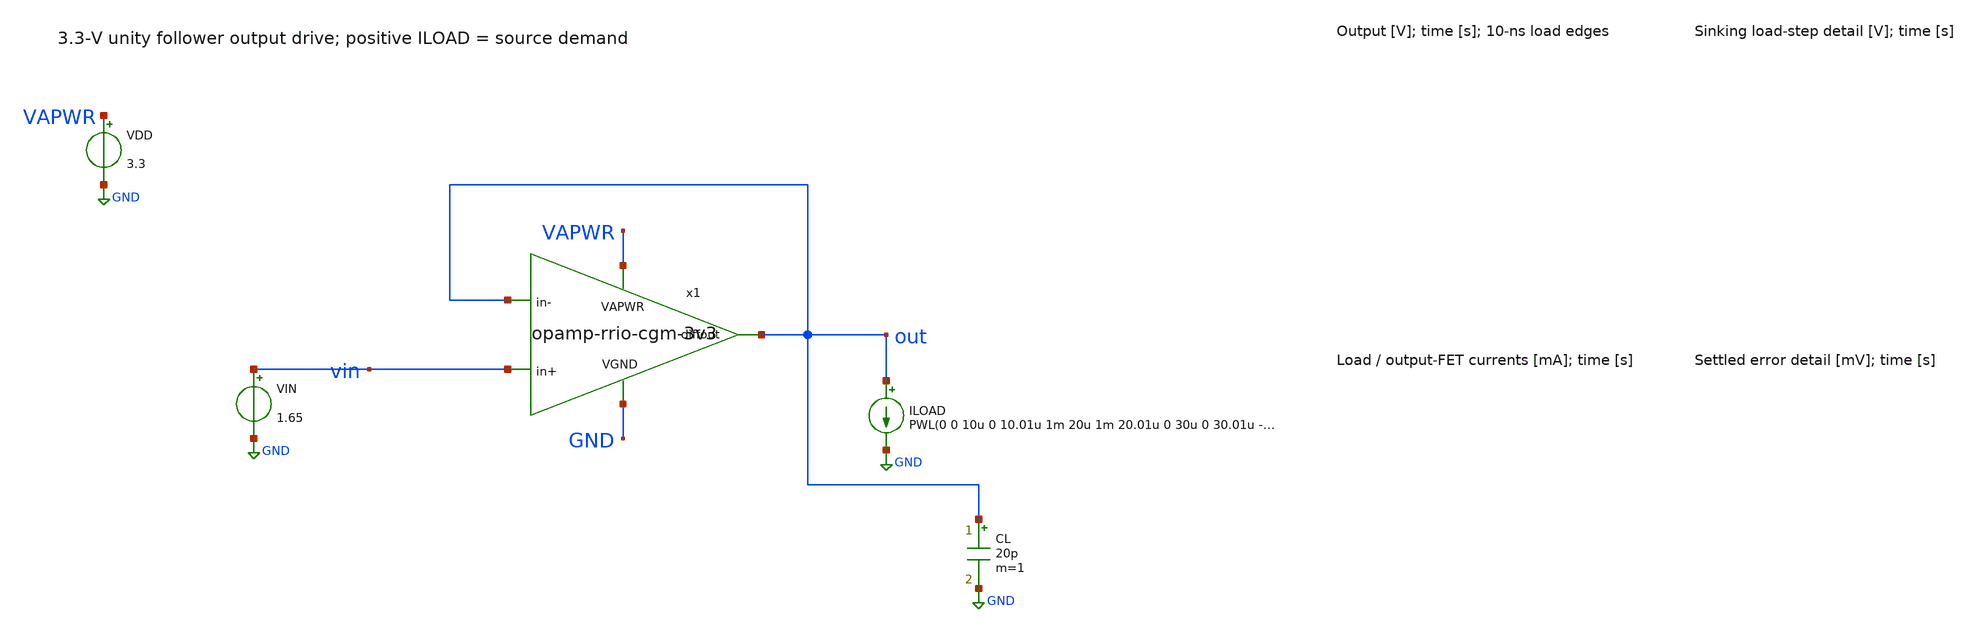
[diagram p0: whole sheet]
** sch_path: xschem/testbench_output_tran_3v3.sch
**.subckt testbench_output_tran_3v3
x1 VAPWR out vin out GND opamp-rrio-cgm-3v3
VDD VAPWR GND 3.3
VIN vin GND 1.65
ILOAD out GND PWL(0 0 10u 0 10.01u 1m 20u 1m 20.01u 0 30u 0 30.01u -1m 40u -1m 40.01u 0 50u 0)
CL out GND 20p m=1
**** begin user architecture code
 .lib $::SKYWATER_MODELS/sky130.lib.spice tt

.options klu itl1=100 reltol=.0001
.nodeset v(x1.net1)=2.55229105
.nodeset v(x1.net3)=0.866789395
.nodeset v(x1.net4)=0.29731059
.nodeset v(x1.net5)=0.297227056
.nodeset v(x1.net10)=2.03109432
.nodeset v(x1.net12)=1.08535928
.nodeset v(x1.net6)=2.02894826
.nodeset v(x1.net13)=1.08255405
.nodeset v(x1.bias1)=2.05405688
.nodeset v(x1.bias2)=2.04452255
.nodeset v(x1.bias3)=1.14047666
.nodeset v(x1.bias4)=1.04710014
.nodeset v(x1.bias)=1.65
.nodeset v(out)=1.65 v(x1.xb.xref.vbiasn)=.91 v(x1.xb.xref.vbiasp)=2.05 v(x1.xb.xref.vstartup)=.1
.control
set wr_singlescale
set wr_vecnames
save all @iload[current] @m.x1.xm29.msky130_fd_pr__pfet_g5v0d10v5[id]
+ @m.x1.xm32.msky130_fd_pr__nfet_g5v0d10v5[id] @m.x1.xb.xref.xm1.msky130_fd_pr__pfet_g5v0d10v5[id]
tran 5n 50u 0 5n

* Reject roots outside the SKY130 HV gate-voltage range.
let physical_bias_peak = vecmax(abs(v(x1.bias)))
if physical_bias_peak > 5.5
echo PHYSICAL_BIAS_ERROR: invalid PDK operating point
quit 1
end
let error_mV=1000*(v(out)-v(vin))
let load_mA=1000*@iload[current]
let source_mA=1000*@m.x1.xm29.msky130_fd_pr__pfet_g5v0d10v5[id]
let sink_mA=1000*@m.x1.xm32.msky130_fd_pr__nfet_g5v0d10v5[id]
write testbench_output_tran_3v3.raw all
wrdata testbench_output_tran_3v3.dat v(vin) v(out) @iload[current] i(VDD)
+ @m.x1.xm29.msky130_fd_pr__pfet_g5v0d10v5[id] @m.x1.xm32.msky130_fd_pr__nfet_g5v0d10v5[id] @m.x1.xb.xref.xm1.msky130_fd_pr__pfet_g5v0d10v5[id]
.endc

**** end user architecture code
**.ends

* expanding   symbol:  opamp-rrio-cgm-3v3.sym # of pins=5
** sym_path: xschem/opamp-rrio-cgm-3v3.sym
** sch_path: xschem/opamp-rrio-cgm-3v3.sch
.subckt opamp-rrio-cgm-3v3 VAPWR diffout in+ in- VGND
*.ipin in-
*.ipin in+
*.opin diffout
*.iopin VAPWR
*.iopin VGND
XM1 net2 in- net3 VGND sky130_fd_pr__nfet_g5v0d10v5 L=0.5 W=69.44 nf=5 ad='int((nf+1)/2) * W/nf * 0.29'
+ as='int((nf+2)/2) * W/nf * 0.29' pd='2*int((nf+1)/2) * (W/nf + 0.29)' ps='2*int((nf+2)/2) * (W/nf + 0.29)'
+ nrd='0.29 / W' nrs='0.29 / W' sa=0 sb=0 sd=0 mult=1 m=1
XM3 drain in+ net3 VGND sky130_fd_pr__nfet_g5v0d10v5 L=0.5 W=69.44 nf=5 ad='int((nf+1)/2) * W/nf * 0.29'
+ as='int((nf+2)/2) * W/nf * 0.29' pd='2*int((nf+1)/2) * (W/nf + 0.29)' ps='2*int((nf+2)/2) * (W/nf + 0.29)'
+ nrd='0.29 / W' nrs='0.29 / W' sa=0 sb=0 sd=0 mult=1 m=1
XM7 drain bias net3 VGND sky130_fd_pr__nfet_g5v0d10v5 L=0.5 W=69.44 nf=5 ad='int((nf+1)/2) * W/nf * 0.29'
+ as='int((nf+2)/2) * W/nf * 0.29' pd='2*int((nf+1)/2) * (W/nf + 0.29)' ps='2*int((nf+2)/2) * (W/nf + 0.29)'
+ nrd='0.29 / W' nrs='0.29 / W' sa=0 sb=0 sd=0 mult=1 m=1
XM8 net2 bias net3 VGND sky130_fd_pr__nfet_g5v0d10v5 L=0.5 W=69.44 nf=5 ad='int((nf+1)/2) * W/nf * 0.29'
+ as='int((nf+2)/2) * W/nf * 0.29' pd='2*int((nf+1)/2) * (W/nf + 0.29)' ps='2*int((nf+2)/2) * (W/nf + 0.29)'
+ nrd='0.29 / W' nrs='0.29 / W' sa=0 sb=0 sd=0 mult=1 m=1
XM18 net13 bias3 net5 VGND sky130_fd_pr__nfet_g5v0d10v5 L=0.5 W=13.89 nf=1 ad='int((nf+1)/2) * W/nf * 0.29'
+ as='int((nf+2)/2) * W/nf * 0.29' pd='2*int((nf+1)/2) * (W/nf + 0.29)' ps='2*int((nf+2)/2) * (W/nf + 0.29)'
+ nrd='0.29 / W' nrs='0.29 / W' sa=0 sb=0 sd=0 mult=1 m=1
XM19 net12 bias3 net4 VGND sky130_fd_pr__nfet_g5v0d10v5 L=0.5 W=13.89 nf=1 ad='int((nf+1)/2) * W/nf * 0.29'
+ as='int((nf+2)/2) * W/nf * 0.29' pd='2*int((nf+1)/2) * (W/nf + 0.29)' ps='2*int((nf+2)/2) * (W/nf + 0.29)'
+ nrd='0.29 / W' nrs='0.29 / W' sa=0 sb=0 sd=0 mult=1 m=1
XM20 net5 net13 VGND VGND sky130_fd_pr__nfet_g5v0d10v5 L=2 W=6.66 nf=2 ad='int((nf+1)/2) * W/nf * 0.29'
+ as='int((nf+2)/2) * W/nf * 0.29' pd='2*int((nf+1)/2) * (W/nf + 0.29)' ps='2*int((nf+2)/2) * (W/nf + 0.29)'
+ nrd='0.29 / W' nrs='0.29 / W' sa=0 sb=0 sd=0 mult=1 m=1
XM21 net4 net13 VGND VGND sky130_fd_pr__nfet_g5v0d10v5 L=2 W=6.66 nf=2 ad='int((nf+1)/2) * W/nf * 0.29'
+ as='int((nf+2)/2) * W/nf * 0.29' pd='2*int((nf+1)/2) * (W/nf + 0.29)' ps='2*int((nf+2)/2) * (W/nf + 0.29)'
+ nrd='0.29 / W' nrs='0.29 / W' sa=0 sb=0 sd=0 mult=1 m=1
XM22 net3 bias4 VGND VGND sky130_fd_pr__nfet_g5v0d10v5 L=6 W=10 nf=1 ad='int((nf+1)/2) * W/nf * 0.29'
+ as='int((nf+2)/2) * W/nf * 0.29' pd='2*int((nf+1)/2) * (W/nf + 0.29)' ps='2*int((nf+2)/2) * (W/nf + 0.29)'
+ nrd='0.29 / W' nrs='0.29 / W' sa=0 sb=0 sd=0 mult=1 m=1
XM25 net8 net8 net11 VGND sky130_fd_pr__nfet_g5v0d10v5 L=0.5 W=13.89 nf=1 ad='int((nf+1)/2) * W/nf * 0.29'
+ as='int((nf+2)/2) * W/nf * 0.29' pd='2*int((nf+1)/2) * (W/nf + 0.29)' ps='2*int((nf+2)/2) * (W/nf + 0.29)'
+ nrd='0.29 / W' nrs='0.29 / W' sa=0 sb=0 sd=0 mult=1 m=1
XM26 net10 net8 net12 VGND sky130_fd_pr__nfet_g5v0d10v5 L=0.5 W=13.89 nf=1 ad='int((nf+1)/2) * W/nf * 0.29'
+ as='int((nf+2)/2) * W/nf * 0.29' pd='2*int((nf+1)/2) * (W/nf + 0.29)' ps='2*int((nf+2)/2) * (W/nf + 0.29)'
+ nrd='0.29 / W' nrs='0.29 / W' sa=0 sb=0 sd=0 mult=1 m=1
XM30 net11 net11 VGND VGND sky130_fd_pr__nfet_g5v0d10v5 L=2 W=6.66 nf=2 ad='int((nf+1)/2) * W/nf * 0.29'
+ as='int((nf+2)/2) * W/nf * 0.29' pd='2*int((nf+1)/2) * (W/nf + 0.29)' ps='2*int((nf+2)/2) * (W/nf + 0.29)'
+ nrd='0.29 / W' nrs='0.29 / W' sa=0 sb=0 sd=0 mult=1 m=1
XM31 net9 bias4 VGND VGND sky130_fd_pr__nfet_g5v0d10v5 L=6 W=10 nf=1 ad='int((nf+1)/2) * W/nf * 0.29'
+ as='int((nf+2)/2) * W/nf * 0.29' pd='2*int((nf+1)/2) * (W/nf + 0.29)' ps='2*int((nf+2)/2) * (W/nf + 0.29)'
+ nrd='0.29 / W' nrs='0.29 / W' sa=0 sb=0 sd=0 mult=1 m=1
XM32 diffout net12 VGND VGND sky130_fd_pr__nfet_g5v0d10v5 L=2 W=133.2 nf=40 ad='int((nf+1)/2) * W/nf * 0.29'
+ as='int((nf+2)/2) * W/nf * 0.29' pd='2*int((nf+1)/2) * (W/nf + 0.29)' ps='2*int((nf+2)/2) * (W/nf + 0.29)'
+ nrd='0.29 / W' nrs='0.29 / W' sa=0 sb=0 sd=0 mult=1 m=1
XC1 diffout drain sky130_fd_pr__cap_mim_m3_1 W=18 L=18 MF=1 m=1
XC2 diffout net4 sky130_fd_pr__cap_mim_m3_1 W=30 L=30 MF=1 m=1
XC2B diffout net4 sky130_fd_pr__cap_mim_m3_1 W=30 L=10 MF=1 m=1
XM13 net1 bias1 VAPWR VAPWR sky130_fd_pr__pfet_g5v0d10v5 L=6 W=33 nf=1 ad='int((nf+1)/2) * W/nf * 0.29'
+ as='int((nf+2)/2) * W/nf * 0.29' pd='2*int((nf+1)/2) * (W/nf + 0.29)' ps='2*int((nf+2)/2) * (W/nf + 0.29)'
+ nrd='0.29 / W' nrs='0.29 / W' sa=0 sb=0 sd=0 mult=1 m=1
XM14 net2 net6 VAPWR VAPWR sky130_fd_pr__pfet_g5v0d10v5 L=2 W=22 nf=2 ad='int((nf+1)/2) * W/nf * 0.29'
+ as='int((nf+2)/2) * W/nf * 0.29' pd='2*int((nf+1)/2) * (W/nf + 0.29)' ps='2*int((nf+2)/2) * (W/nf + 0.29)'
+ nrd='0.29 / W' nrs='0.29 / W' sa=0 sb=0 sd=0 mult=1 m=1
XM15 drain net6 VAPWR VAPWR sky130_fd_pr__pfet_g5v0d10v5 L=2 W=22 nf=2 ad='int((nf+1)/2) * W/nf * 0.29'
+ as='int((nf+2)/2) * W/nf * 0.29' pd='2*int((nf+1)/2) * (W/nf + 0.29)' ps='2*int((nf+2)/2) * (W/nf + 0.29)'
+ nrd='0.29 / W' nrs='0.29 / W' sa=0 sb=0 sd=0 mult=1 m=1
XM16 net10 bias2 drain VAPWR sky130_fd_pr__pfet_g5v0d10v5 L=0.5 W=45.83 nf=1 ad='int((nf+1)/2) * W/nf * 0.29'
+ as='int((nf+2)/2) * W/nf * 0.29' pd='2*int((nf+1)/2) * (W/nf + 0.29)' ps='2*int((nf+2)/2) * (W/nf + 0.29)'
+ nrd='0.29 / W' nrs='0.29 / W' sa=0 sb=0 sd=0 mult=1 m=1
XM23 net8 bias1 VAPWR VAPWR sky130_fd_pr__pfet_g5v0d10v5 L=6 W=33 nf=1 ad='int((nf+1)/2) * W/nf * 0.29'
+ as='int((nf+2)/2) * W/nf * 0.29' pd='2*int((nf+1)/2) * (W/nf + 0.29)' ps='2*int((nf+2)/2) * (W/nf + 0.29)'
+ nrd='0.29 / W' nrs='0.29 / W' sa=0 sb=0 sd=0 mult=1 m=1
XM24 net6 bias2 net2 VAPWR sky130_fd_pr__pfet_g5v0d10v5 L=0.5 W=45.83 nf=1 ad='int((nf+1)/2) * W/nf * 0.29'
+ as='int((nf+2)/2) * W/nf * 0.29' pd='2*int((nf+1)/2) * (W/nf + 0.29)' ps='2*int((nf+2)/2) * (W/nf + 0.29)'
+ nrd='0.29 / W' nrs='0.29 / W' sa=0 sb=0 sd=0 mult=1 m=1
XM28 net7 net7 VAPWR VAPWR sky130_fd_pr__pfet_g5v0d10v5 L=2 W=22 nf=2 ad='int((nf+1)/2) * W/nf * 0.29'
+ as='int((nf+2)/2) * W/nf * 0.29' pd='2*int((nf+1)/2) * (W/nf + 0.29)' ps='2*int((nf+2)/2) * (W/nf + 0.29)'
+ nrd='0.29 / W' nrs='0.29 / W' sa=0 sb=0 sd=0 mult=1 m=1
XM29 diffout net10 VAPWR VAPWR sky130_fd_pr__pfet_g5v0d10v5 L=2 W=440 nf=40 ad='int((nf+1)/2) * W/nf * 0.29'
+ as='int((nf+2)/2) * W/nf * 0.29' pd='2*int((nf+1)/2) * (W/nf + 0.29)' ps='2*int((nf+2)/2) * (W/nf + 0.29)'
+ nrd='0.29 / W' nrs='0.29 / W' sa=0 sb=0 sd=0 mult=1 m=1
XM34 net9 net9 net7 VAPWR sky130_fd_pr__pfet_g5v0d10v5 L=0.5 W=45.83 nf=1 ad='int((nf+1)/2) * W/nf * 0.29'
+ as='int((nf+2)/2) * W/nf * 0.29' pd='2*int((nf+1)/2) * (W/nf + 0.29)' ps='2*int((nf+2)/2) * (W/nf + 0.29)'
+ nrd='0.29 / W' nrs='0.29 / W' sa=0 sb=0 sd=0 mult=1 m=1
XM35 net12 net9 net10 VAPWR sky130_fd_pr__pfet_g5v0d10v5 L=0.5 W=45.83 nf=1 ad='int((nf+1)/2) * W/nf * 0.29'
+ as='int((nf+2)/2) * W/nf * 0.29' pd='2*int((nf+1)/2) * (W/nf + 0.29)' ps='2*int((nf+2)/2) * (W/nf + 0.29)'
+ nrd='0.29 / W' nrs='0.29 / W' sa=0 sb=0 sd=0 mult=1 m=1
XM2 net4 bias net1 VAPWR sky130_fd_pr__pfet_g5v0d10v5 L=0.5 W=229.17 nf=10 ad='int((nf+1)/2) * W/nf * 0.29'
+ as='int((nf+2)/2) * W/nf * 0.29' pd='2*int((nf+1)/2) * (W/nf + 0.29)' ps='2*int((nf+2)/2) * (W/nf + 0.29)'
+ nrd='0.29 / W' nrs='0.29 / W' sa=0 sb=0 sd=0 mult=2 m=2
XM4 net5 bias net1 VAPWR sky130_fd_pr__pfet_g5v0d10v5 L=0.5 W=229.17 nf=10 ad='int((nf+1)/2) * W/nf * 0.29'
+ as='int((nf+2)/2) * W/nf * 0.29' pd='2*int((nf+1)/2) * (W/nf + 0.29)' ps='2*int((nf+2)/2) * (W/nf + 0.29)'
+ nrd='0.29 / W' nrs='0.29 / W' sa=0 sb=0 sd=0 mult=2 m=2
XM9 net5 in- net1 VAPWR sky130_fd_pr__pfet_g5v0d10v5 L=0.5 W=229.17 nf=10 ad='int((nf+1)/2) * W/nf * 0.29'
+ as='int((nf+2)/2) * W/nf * 0.29' pd='2*int((nf+1)/2) * (W/nf + 0.29)' ps='2*int((nf+2)/2) * (W/nf + 0.29)'
+ nrd='0.29 / W' nrs='0.29 / W' sa=0 sb=0 sd=0 mult=2 m=2
XM10 net4 in+ net1 VAPWR sky130_fd_pr__pfet_g5v0d10v5 L=0.5 W=229.17 nf=10 ad='int((nf+1)/2) * W/nf * 0.29'
+ as='int((nf+2)/2) * W/nf * 0.29' pd='2*int((nf+1)/2) * (W/nf + 0.29)' ps='2*int((nf+2)/2) * (W/nf + 0.29)'
+ nrd='0.29 / W' nrs='0.29 / W' sa=0 sb=0 sd=0 mult=2 m=2
XB VAPWR VGND bias1 bias4 bias2 bias3 bias opamp_bias_3v3
XMFC_P net13 net9 net6 VAPWR sky130_fd_pr__pfet_g5v0d10v5 L=0.5 W=45.83 nf=1 ad='int((nf+1)/2) * W/nf * 0.29'
+ as='int((nf+2)/2) * W/nf * 0.29' pd='2*int((nf+1)/2) * (W/nf + 0.29)' ps='2*int((nf+2)/2) * (W/nf + 0.29)'
+ nrd='0.29 / W' nrs='0.29 / W' sa=0 sb=0 sd=0 mult=1 m=1
XMFC_N net6 net8 net13 VGND sky130_fd_pr__nfet_g5v0d10v5 L=0.5 W=13.89 nf=1 ad='int((nf+1)/2) * W/nf * 0.29'
+ as='int((nf+2)/2) * W/nf * 0.29' pd='2*int((nf+1)/2) * (W/nf + 0.29)' ps='2*int((nf+2)/2) * (W/nf + 0.29)'
+ nrd='0.29 / W' nrs='0.29 / W' sa=0 sb=0 sd=0 mult=1 m=1
.ends


* expanding   symbol:  opamp_bias_3v3.sym # of pins=7
** sym_path: xschem/opamp_bias_3v3.sym
** sch_path: xschem/opamp_bias_3v3.sch
.subckt opamp_bias_3v3 VAPWR VGND bias1 bias4 bias2 bias3 bias
*.iopin VAPWR
*.iopin VGND
*.opin bias1
*.opin bias4
*.opin bias2
*.opin bias3
*.opin bias
XREF VAPWR IREF VGND reference_bias_3v3
XMBN IREF IREF VGND VGND sky130_fd_pr__nfet_g5v0d10v5 L=1 W=5 nf=1 ad='int((nf+1)/2) * W/nf * 0.29' as='int((nf+2)/2) * W/nf * 0.29'
+ pd='2*int((nf+1)/2) * (W/nf + 0.29)' ps='2*int((nf+2)/2) * (W/nf + 0.29)' nrd='0.29 / W' nrs='0.29 / W'
+ sa=0 sb=0 sd=0 mult=1 m=1
XMPMASTER PMASTER PMASTER VAPWR VAPWR sky130_fd_pr__pfet_g5v0d10v5 L=1 W=10 nf=1 ad='int((nf+1)/2) * W/nf * 0.29'
+ as='int((nf+2)/2) * W/nf * 0.29' pd='2*int((nf+1)/2) * (W/nf + 0.29)' ps='2*int((nf+2)/2) * (W/nf + 0.29)'
+ nrd='0.29 / W' nrs='0.29 / W' sa=0 sb=0 sd=0 mult=1 m=1
XMNMASTER PMASTER IREF VGND VGND sky130_fd_pr__nfet_g5v0d10v5 L=1 W=5 nf=1 ad='int((nf+1)/2) * W/nf * 0.29'
+ as='int((nf+2)/2) * W/nf * 0.29' pd='2*int((nf+1)/2) * (W/nf + 0.29)' ps='2*int((nf+2)/2) * (W/nf + 0.29)'
+ nrd='0.29 / W' nrs='0.29 / W' sa=0 sb=0 sd=0 mult=1 m=1
XMPTAIL bias1 bias1 VAPWR VAPWR sky130_fd_pr__pfet_g5v0d10v5 L=6 W=33 nf=1 ad='int((nf+1)/2) * W/nf * 0.29'
+ as='int((nf+2)/2) * W/nf * 0.29' pd='2*int((nf+1)/2) * (W/nf + 0.29)' ps='2*int((nf+2)/2) * (W/nf + 0.29)'
+ nrd='0.29 / W' nrs='0.29 / W' sa=0 sb=0 sd=0 mult=1 m=1
XMNPTAIL bias1 IREF VGND VGND sky130_fd_pr__nfet_g5v0d10v5 L=1 W=5 nf=1 ad='int((nf+1)/2) * W/nf * 0.29'
+ as='int((nf+2)/2) * W/nf * 0.29' pd='2*int((nf+1)/2) * (W/nf + 0.29)' ps='2*int((nf+2)/2) * (W/nf + 0.29)'
+ nrd='0.29 / W' nrs='0.29 / W' sa=0 sb=0 sd=0 mult=1 m=1
XMPNTAIL bias4 PMASTER VAPWR VAPWR sky130_fd_pr__pfet_g5v0d10v5 L=1 W=10 nf=1 ad='int((nf+1)/2) * W/nf * 0.29'
+ as='int((nf+2)/2) * W/nf * 0.29' pd='2*int((nf+1)/2) * (W/nf + 0.29)' ps='2*int((nf+2)/2) * (W/nf + 0.29)'
+ nrd='0.29 / W' nrs='0.29 / W' sa=0 sb=0 sd=0 mult=1 m=1
XMNTAIL bias4 bias4 VGND VGND sky130_fd_pr__nfet_g5v0d10v5 L=6 W=10 nf=1 ad='int((nf+1)/2) * W/nf * 0.29'
+ as='int((nf+2)/2) * W/nf * 0.29' pd='2*int((nf+1)/2) * (W/nf + 0.29)' ps='2*int((nf+2)/2) * (W/nf + 0.29)'
+ nrd='0.29 / W' nrs='0.29 / W' sa=0 sb=0 sd=0 mult=1 m=1
XRPCAS PCAS_SOURCE VAPWR VGND sky130_fd_pr__res_high_po_0p69 L=100 mult=1 m=1
XMPCAS bias2 bias2 PCAS_SOURCE VAPWR sky130_fd_pr__pfet_g5v0d10v5 L=0.5 W=45.83 nf=1 ad='int((nf+1)/2) * W/nf * 0.29'
+ as='int((nf+2)/2) * W/nf * 0.29' pd='2*int((nf+1)/2) * (W/nf + 0.29)' ps='2*int((nf+2)/2) * (W/nf + 0.29)'
+ nrd='0.29 / W' nrs='0.29 / W' sa=0 sb=0 sd=0 mult=1 m=1
XMNPCAS bias2 IREF VGND VGND sky130_fd_pr__nfet_g5v0d10v5 L=1 W=5 nf=1 ad='int((nf+1)/2) * W/nf * 0.29'
+ as='int((nf+2)/2) * W/nf * 0.29' pd='2*int((nf+1)/2) * (W/nf + 0.29)' ps='2*int((nf+2)/2) * (W/nf + 0.29)'
+ nrd='0.29 / W' nrs='0.29 / W' sa=0 sb=0 sd=0 mult=1 m=1
XMPNCAS bias3 PMASTER VAPWR VAPWR sky130_fd_pr__pfet_g5v0d10v5 L=1 W=10 nf=1 ad='int((nf+1)/2) * W/nf * 0.29'
+ as='int((nf+2)/2) * W/nf * 0.29' pd='2*int((nf+1)/2) * (W/nf + 0.29)' ps='2*int((nf+2)/2) * (W/nf + 0.29)'
+ nrd='0.29 / W' nrs='0.29 / W' sa=0 sb=0 sd=0 mult=1 m=1
XMNCAS bias3 bias3 NCAS_SOURCE VGND sky130_fd_pr__nfet_g5v0d10v5 L=0.5 W=13.89 nf=1 ad='int((nf+1)/2) * W/nf * 0.29'
+ as='int((nf+2)/2) * W/nf * 0.29' pd='2*int((nf+1)/2) * (W/nf + 0.29)' ps='2*int((nf+2)/2) * (W/nf + 0.29)'
+ nrd='0.29 / W' nrs='0.29 / W' sa=0 sb=0 sd=0 mult=1 m=1
XRNCAS VGND NCAS_SOURCE VGND sky130_fd_pr__res_high_po_0p69 L=100 mult=1 m=1
XRCM_TOP bias VAPWR VGND sky130_fd_pr__res_high_po_0p69 L=150 mult=1 m=1
XRCM_BOTTOM VGND bias VGND sky130_fd_pr__res_high_po_0p69 L=150 mult=1 m=1
.ends


* expanding   symbol:  reference_bias_3v3.sym # of pins=3
** sym_path: xschem/reference_bias_3v3.sym
** sch_path: xschem/reference_bias_3v3.sch
.subckt reference_bias_3v3 VAPWR IREF VGND
*.iopin VAPWR
*.iopin VGND
*.opin IREF
XR1 VGND net1 VGND sky130_fd_pr__res_high_po_0p69 L=30.5 mult=1 m=1
XM40 Vbiasp Vbiasp VAPWR VAPWR sky130_fd_pr__pfet_g5v0d10v5 L=1 W=10 nf=1 ad='int((nf+1)/2) * W/nf * 0.29'
+ as='int((nf+2)/2) * W/nf * 0.29' pd='2*int((nf+1)/2) * (W/nf + 0.29)' ps='2*int((nf+2)/2) * (W/nf + 0.29)'
+ nrd='0.29 / W' nrs='0.29 / W' sa=0 sb=0 sd=0 mult=1 m=1
XM44 Vstartup Vbiasn VGND VGND sky130_fd_pr__nfet_g5v0d10v5 L=1 W=3 nf=1 ad='int((nf+1)/2) * W/nf * 0.29'
+ as='int((nf+2)/2) * W/nf * 0.29' pd='2*int((nf+1)/2) * (W/nf + 0.29)' ps='2*int((nf+2)/2) * (W/nf + 0.29)'
+ nrd='0.29 / W' nrs='0.29 / W' sa=0 sb=0 sd=0 mult=1 m=1
XM41 Vbiasn Vbiasp VAPWR VAPWR sky130_fd_pr__pfet_g5v0d10v5 L=1 W=10 nf=1 ad='int((nf+1)/2) * W/nf * 0.29'
+ as='int((nf+2)/2) * W/nf * 0.29' pd='2*int((nf+1)/2) * (W/nf + 0.29)' ps='2*int((nf+2)/2) * (W/nf + 0.29)'
+ nrd='0.29 / W' nrs='0.29 / W' sa=0 sb=0 sd=0 mult=1 m=1
XM43 Vstartup Vstartup VAPWR VAPWR sky130_fd_pr__pfet_g5v0d10v5 L=10 W=1 nf=1 ad='int((nf+1)/2) * W/nf * 0.29'
+ as='int((nf+2)/2) * W/nf * 0.29' pd='2*int((nf+1)/2) * (W/nf + 0.29)' ps='2*int((nf+2)/2) * (W/nf + 0.29)'
+ nrd='0.29 / W' nrs='0.29 / W' sa=0 sb=0 sd=0 mult=1 m=1
XM42 Vbiasn Vbiasn VGND VGND sky130_fd_pr__nfet_g5v0d10v5 L=1 W=5 nf=1 ad='int((nf+1)/2) * W/nf * 0.29'
+ as='int((nf+2)/2) * W/nf * 0.29' pd='2*int((nf+1)/2) * (W/nf + 0.29)' ps='2*int((nf+2)/2) * (W/nf + 0.29)'
+ nrd='0.29 / W' nrs='0.29 / W' sa=0 sb=0 sd=0 mult=1 m=1
XM39 Vbiasp Vbiasn net1 VGND sky130_fd_pr__nfet_g5v0d10v5 L=1 W=20 nf=1 ad='int((nf+1)/2) * W/nf * 0.29'
+ as='int((nf+2)/2) * W/nf * 0.29' pd='2*int((nf+1)/2) * (W/nf + 0.29)' ps='2*int((nf+2)/2) * (W/nf + 0.29)'
+ nrd='0.29 / W' nrs='0.29 / W' sa=0 sb=0 sd=0 mult=1 m=1
XM45 Vbiasp Vstartup Vbiasn VGND sky130_fd_pr__nfet_g5v0d10v5 L=1 W=2 nf=1 ad='int((nf+1)/2) * W/nf * 0.29'
+ as='int((nf+2)/2) * W/nf * 0.29' pd='2*int((nf+1)/2) * (W/nf + 0.29)' ps='2*int((nf+2)/2) * (W/nf + 0.29)'
+ nrd='0.29 / W' nrs='0.29 / W' sa=0 sb=0 sd=0 mult=1 m=1
XM1 IREF Vbiasp VAPWR VAPWR sky130_fd_pr__pfet_g5v0d10v5 L=1 W=10 nf=1 ad='int((nf+1)/2) * W/nf * 0.29'
+ as='int((nf+2)/2) * W/nf * 0.29' pd='2*int((nf+1)/2) * (W/nf + 0.29)' ps='2*int((nf+2)/2) * (W/nf + 0.29)'
+ nrd='0.29 / W' nrs='0.29 / W' sa=0 sb=0 sd=0 mult=1 m=1
.ends

.GLOBAL GND
.end
